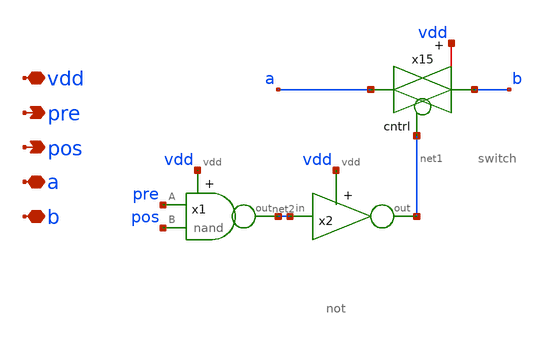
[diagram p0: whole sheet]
** sch_path: designs/subcells/core_synpCntrl/synpCntrl.sch
**.subckt synpCntrl pre pos a b vdd
*.opin pre
*.opin pos
*.iopin a
*.iopin b
*.iopin vdd
x15 net1 b a vdd switch
x1 vdd net2 pre pos nand
x2 vdd net2 net1 not
**.ends

* expanding   symbol:  /foss/designs/spike_130/designs/subcells/core_switch/switch.sym # of pins=4
** sym_path: designs/subcells/core_switch/switch.sym
** sch_path: designs/subcells/core_switch/switch.sch
.subckt switch cntrl in out vdd
*.ipin cntrl
*.ipin in
*.iopin vdd
*.opin out
XM3 out cntrl in GND sky130_fd_pr__nfet_01v8 L=0.15 W=1 nf=1 ad='int((1 + 1)/2) * 1 / 1 * 0.29' as='int((1 + 2)/2) * 1 / 1 * 0.29'
+ pd='2*int((1 + 1)/2) * (1 / 1 + 0.29)' ps='2*int((1 + 2)/2) * (1 / 1 + 0.29)' nrd='0.29 / 1 ' nrs='0.29 / 1 '
+ sa=0 sb=0 sd=0 mult=1 m=1
XM4 out net1 in vdd sky130_fd_pr__pfet_01v8 L=0.15 W=1 nf=1 ad='int((nf+1)/2) * W/nf * 0.29' as='int((nf+2)/2) * W/nf * 0.29'
+ pd='2*int((nf+1)/2) * (W/nf + 0.29)' ps='2*int((nf+2)/2) * (W/nf + 0.29)' nrd='0.29 / W' nrs='0.29 / W'
+ sa=0 sb=0 sd=0 mult=1 m=1
x1 vdd cntrl net1 not
.ends


* expanding   symbol:  /foss/designs/spike_130/designs/subcells/core_nand/nand.sym # of pins=4
** sym_path: designs/subcells/core_nand/nand.sym
** sch_path: designs/subcells/core_nand/nand.sch
.subckt nand vdd out A B
*.iopin vdd
*.opin out
*.ipin A
*.ipin B
XM4 net1 B GND GND sky130_fd_pr__nfet_01v8_lvt L=0.15 W=1 nf=1 ad='int((1 + 1)/2) * 1 / 1 * 0.29' as='int((1 + 2)/2) * 1 / 1 * 0.29'
+ pd='2*int((1 + 1)/2) * (1 / 1 + 0.29)' ps='2*int((1 + 2)/2) * (1 / 1 + 0.29)' nrd='0.29 / 1 ' nrs='0.29 / 1 '
+ sa=0 sb=0 sd=0 mult=1 m=1
XM1 out B vdd vdd sky130_fd_pr__pfet_01v8_lvt L=0.35 W=1 nf=1 ad='int((1 + 1)/2) * 1 / 1 * 0.29' as='int((1 + 2)/2) * 1 / 1 * 0.29'
+ pd='2*int((1 + 1)/2) * (1 / 1 + 0.29)' ps='2*int((1 + 2)/2) * (1 / 1 + 0.29)' nrd='0.29 / 1 ' nrs='0.29 / 1 '
+ sa=0 sb=0 sd=0 mult=1 m=1
XM2 out A vdd vdd sky130_fd_pr__pfet_01v8_lvt L=0.35 W=1 nf=1 ad='int((1 + 1)/2) * 1 / 1 * 0.29' as='int((1 + 2)/2) * 1 / 1 * 0.29'
+ pd='2*int((1 + 1)/2) * (1 / 1 + 0.29)' ps='2*int((1 + 2)/2) * (1 / 1 + 0.29)' nrd='0.29 / 1 ' nrs='0.29 / 1 '
+ sa=0 sb=0 sd=0 mult=1 m=1
XM3 out A net1 GND sky130_fd_pr__nfet_01v8_lvt L=0.15 W=1 nf=1 ad='int((1 + 1)/2) * 1 / 1 * 0.29' as='int((1 + 2)/2) * 1 / 1 * 0.29'
+ pd='2*int((1 + 1)/2) * (1 / 1 + 0.29)' ps='2*int((1 + 2)/2) * (1 / 1 + 0.29)' nrd='0.29 / 1 ' nrs='0.29 / 1 '
+ sa=0 sb=0 sd=0 mult=1 m=1
.ends


* expanding   symbol:  /foss/designs/spike_130/designs/subcells/core_not/not.sym # of pins=3
** sym_path: designs/subcells/core_not/not.sym
** sch_path: designs/subcells/core_not/not.sch
.subckt not vdd in out
*.ipin in
*.opin out
*.iopin vdd
XM10 out in vdd vdd sky130_fd_pr__pfet_01v8_lvt L=0.35 W=1 nf=1 ad='int((1 + 1)/2) * 1 / 1 * 0.29' as='int((1 + 2)/2) * 1 / 1 * 0.29'
+ pd='2*int((1 + 1)/2) * (1 / 1 + 0.29)' ps='2*int((1 + 2)/2) * (1 / 1 + 0.29)' nrd='0.29 / 1 ' nrs='0.29 / 1 '
+ sa=0 sb=0 sd=0 mult=1 m=1
XM1 out in GND GND sky130_fd_pr__nfet_01v8_lvt L=0.15 W=1 nf=1 ad='int((1 + 1)/2) * 1 / 1 * 0.29' as='int((1 + 2)/2) * 1 / 1 * 0.29'
+ pd='2*int((1 + 1)/2) * (1 / 1 + 0.29)' ps='2*int((1 + 2)/2) * (1 / 1 + 0.29)' nrd='0.29 / 1 ' nrs='0.29 / 1 '
+ sa=0 sb=0 sd=0 mult=1 m=1
.ends

.GLOBAL GND
.end
